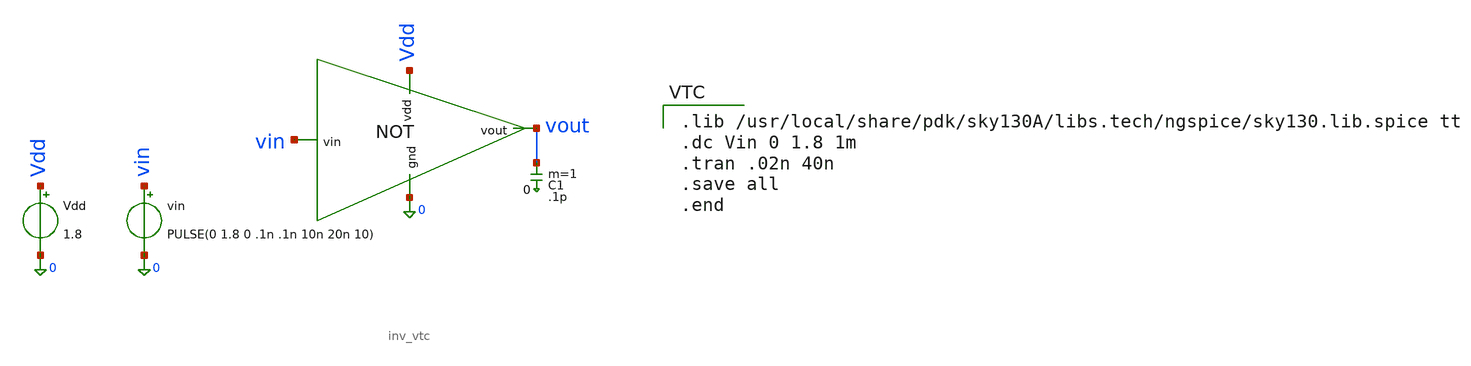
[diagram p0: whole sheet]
** sch_path: cmos_inverter_vtc/inv_test.sch
**.subckt inv_test
x1 vin Vdd 0 vout inv_vtc
vin vin 0 PULSE(0 1.8 0 .1n .1n 10n 20n 10)
Vdd Vdd 0 1.8
C1 vout 0 .1p m=1
**** begin user architecture code

.lib /usr/local/share/pdk/sky130A/libs.tech/ngspice/sky130.lib.spice tt
.dc Vin 0 1.8 1m
.tran .02n 40n
.save all
.end

**** end user architecture code
**.ends

* expanding   symbol:  inv_vtc.sym # of pins=4
** sym_path: cmos_inverter_vtc/inv_vtc.sym
** sch_path: cmos_inverter_vtc/inv_vtc.sch
.subckt inv_vtc vin vdd gnd vout
*.ipin vin
*.ipin vdd
*.ipin gnd
*.opin vout
XM1 vout vin gnd gnd sky130_fd_pr__nfet_01v8 L=0.15 W=1 nf=1 ad='int((1 + 1)/2) * 1 / 1 * 0.29' as='int((1 + 2)/2) * 1 / 1 * 0.29'
+ pd='2*int((1 + 1)/2) * (1 / 1 + 0.29)' ps='2*int((1 + 2)/2) * (1 / 1 + 0.29)' nrd='0.29 / 1 ' nrs='0.29 / 1 '
+ sa=0 sb=0 sd=0 mult=1 m=1
XM2 vout vin vdd vdd sky130_fd_pr__pfet_01v8 L=0.15 W=2 nf=1 ad='int((1 + 1)/2) * 2 / 1 * 0.29' as='int((1 + 2)/2) * 2 / 1 * 0.29'
+ pd='2*int((1 + 1)/2) * (2 / 1 + 0.29)' ps='2*int((1 + 2)/2) * (2 / 1 + 0.29)' nrd='0.29 / 2 ' nrs='0.29 / 2 '
+ sa=0 sb=0 sd=0 mult=1 m=1
.ends

.end
